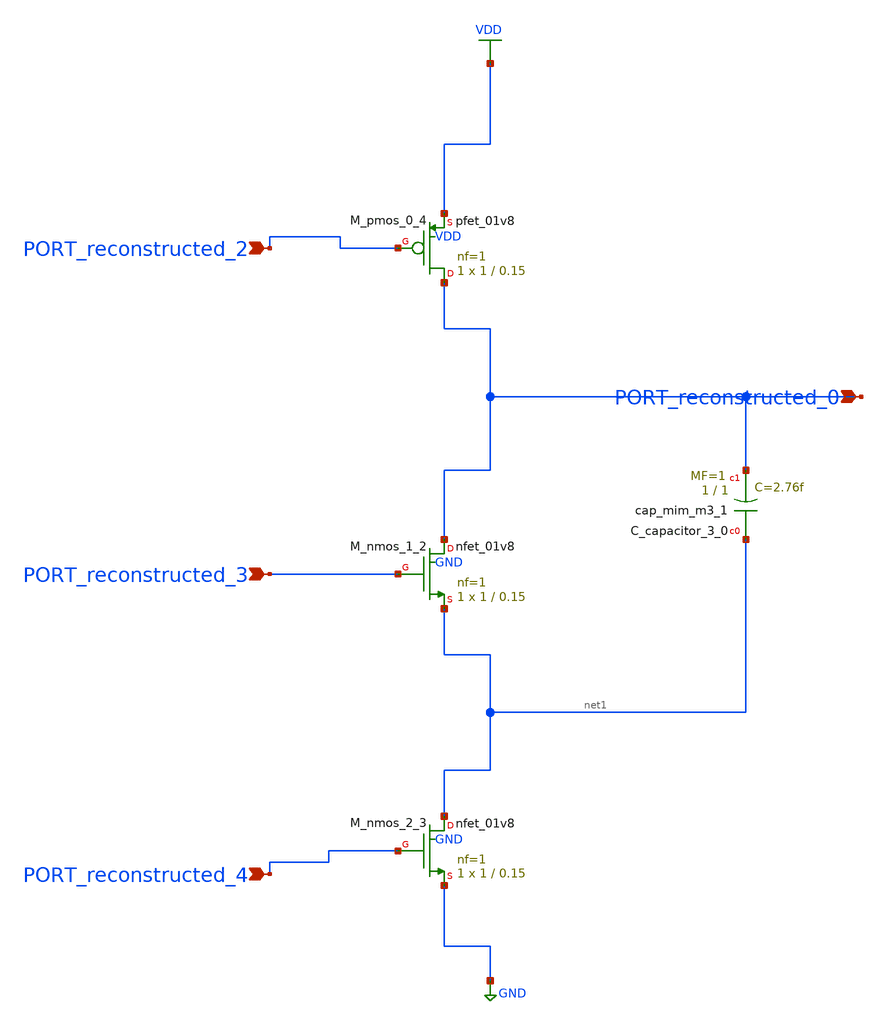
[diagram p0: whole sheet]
** sch_path: schematics/AMSNet/418.sch
**.subckt 418 PORT_reconstructed_2 PORT_reconstructed_3 PORT_reconstructed_4 PORT_reconstructed_0
*.ipin PORT_reconstructed_2
*.ipin PORT_reconstructed_3
*.ipin PORT_reconstructed_4
*.ipin PORT_reconstructed_0
XC_capacitor_3_0 net1 PORT_reconstructed_0 sky130_fd_pr__cap_mim_m3_1 W=1 L=1 MF=1 m=1
XM_nmos_1_2 PORT_reconstructed_0 PORT_reconstructed_3 net1 GND sky130_fd_pr__nfet_01v8 L=0.15 W=1 nf=1
+ ad='int((1 + 1)/2) * 1 / 1 * 0.29' as='int((1 + 2)/2) * 1 / 1 * 0.29' pd='2*int((1 + 1)/2) * (1 / 1 + 0.29)'
+ ps='2*int((1 + 2)/2) * (1 / 1 + 0.29)' nrd='0.29 / 1 ' nrs='0.29 / 1 ' sa=0 sb=0 sd=0 mult=1 m=1
XM_nmos_2_3 net1 PORT_reconstructed_4 GND GND sky130_fd_pr__nfet_01v8 L=0.15 W=1 nf=1 ad='int((1 + 1)/2) * 1 / 1 * 0.29'
+ as='int((1 + 2)/2) * 1 / 1 * 0.29' pd='2*int((1 + 1)/2) * (1 / 1 + 0.29)' ps='2*int((1 + 2)/2) * (1 / 1 + 0.29)'
+ nrd='0.29 / 1 ' nrs='0.29 / 1 ' sa=0 sb=0 sd=0 mult=1 m=1
XM_pmos_0_4 PORT_reconstructed_0 PORT_reconstructed_2 VDD VDD sky130_fd_pr__pfet_01v8 L=0.15 W=1 nf=1
+ ad='int((1 + 1)/2) * 1 / 1 * 0.29' as='int((1 + 2)/2) * 1 / 1 * 0.29' pd='2*int((1 + 1)/2) * (1 / 1 + 0.29)'
+ ps='2*int((1 + 2)/2) * (1 / 1 + 0.29)' nrd='0.29 / 1 ' nrs='0.29 / 1 ' sa=0 sb=0 sd=0 mult=1 m=1
**.ends
.GLOBAL GND
.GLOBAL VDD
.end
